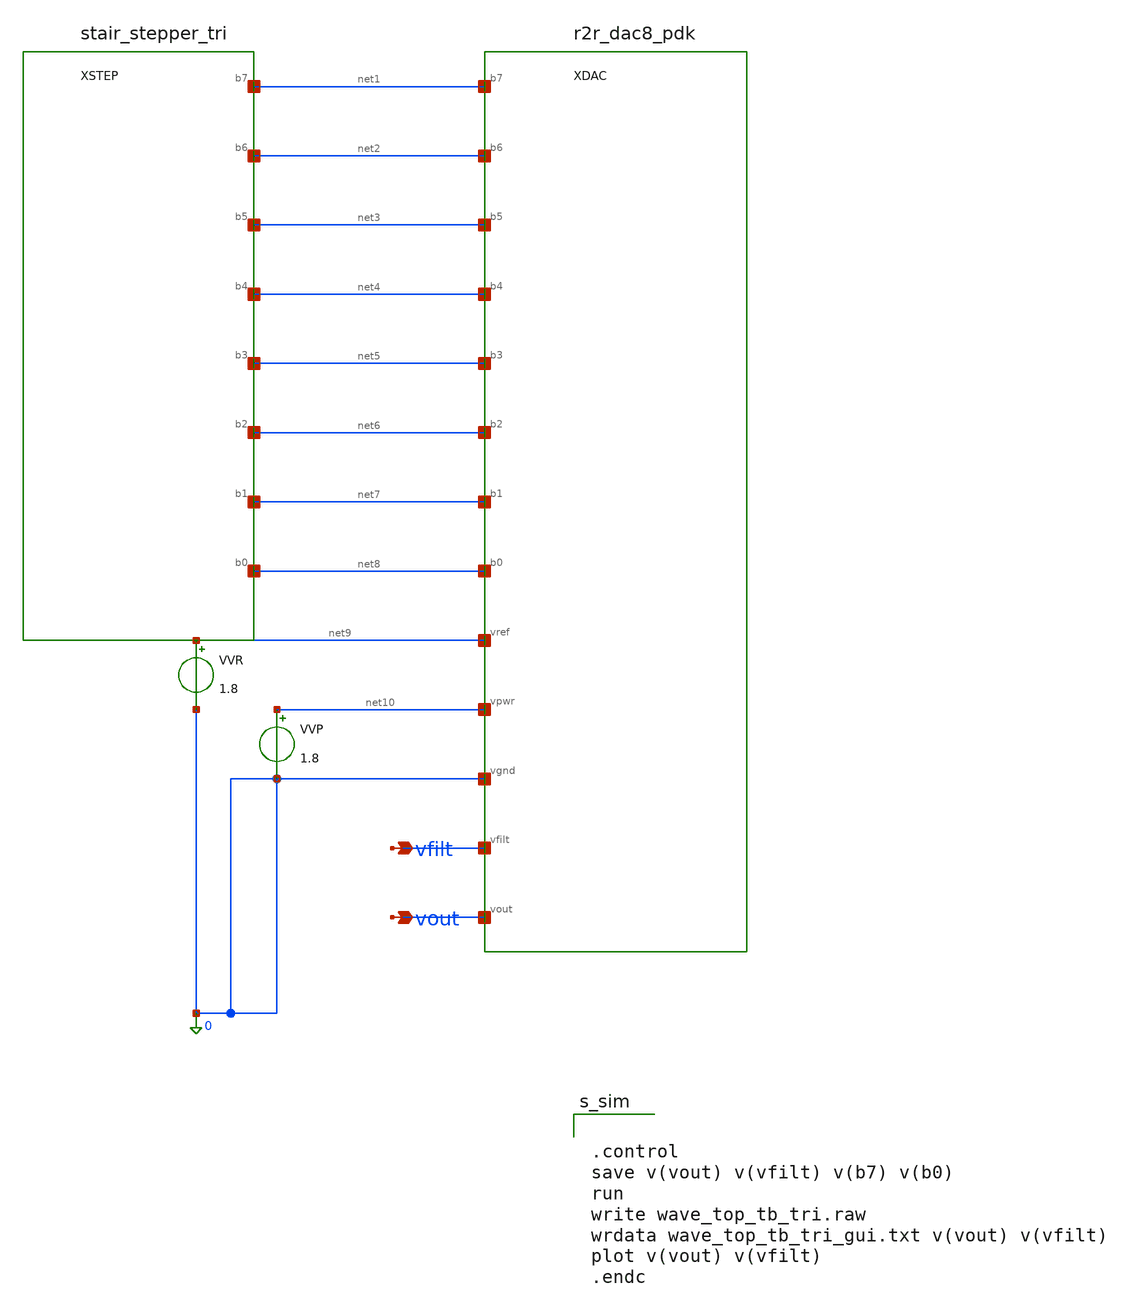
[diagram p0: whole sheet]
** sch_path: design/analog/xschem/wave_top_tb_tri.sch
**.subckt wave_top_tb_tri vfilt vout
*.opin vfilt
*.opin vout
XDAC net1 net2 net3 net4 net5 net6 net7 net8 net9 net10 0 vfilt vout r2r_dac8_pdk
XSTEP net1 net2 net3 net4 net5 net6 net7 net8 stair_stepper_tri
VVR net9 0 1.8
VVP net10 0 1.8
**** begin user architecture code

.lib /home/alrida-ismail/.local/share/pdk/sky130A/libs.tech/ngspice/sky130.lib.spice tt


.tran 100p 5.12e-06)


* tb: 256clk staircase replay of the RTL golden (see gen_tb_sch.py). Ctrl+click the launcher to load
*+ wave_top_tb_tri.raw into the embedded graph; batch proof (make tbexpand) reproduces results/tb_replay_tri.txt
*+ bit-identically



.control
save v(vout) v(vfilt) v(b7) v(b0)
run
write wave_top_tb_tri.raw
wrdata wave_top_tb_tri_gui.txt v(vout) v(vfilt)
plot v(vout) v(vfilt)
.endc


**** end user architecture code
**.ends

* expanding   symbol:  r2r_dac8_pdk.sym # of pins=13
** sym_path: design/analog/xschem/r2r_dac8_pdk.sym
** sch_path: design/analog/xschem/r2r_dac8_pdk.sch
.subckt r2r_dac8_pdk b7 b6 b5 b4 b3 b2 b1 b0 vref vpwr vgnd vfilt vout
*.ipin b7
*.ipin b6
*.ipin b5
*.ipin b4
*.ipin b3
*.ipin b2
*.ipin b1
*.ipin b0
*.ipin vref
*.ipin vpwr
*.ipin vgnd
*.opin vfilt
*.opin vout
XR76 n6 vout vgnd sky130_fd_pr__res_high_po W=4 L=357.43 mult=1 m=1
XR65 n5 n6 vgnd sky130_fd_pr__res_high_po W=4 L=357.43 mult=1 m=1
XR54 n4 n5 vgnd sky130_fd_pr__res_high_po W=4 L=357.43 mult=1 m=1
XR43 n3 n4 vgnd sky130_fd_pr__res_high_po W=4 L=357.43 mult=1 m=1
XR32 n2 n3 vgnd sky130_fd_pr__res_high_po W=4 L=357.43 mult=1 m=1
XR21 n1 n2 vgnd sky130_fd_pr__res_high_po W=4 L=357.43 mult=1 m=1
XR10 n0 n1 vgnd sky130_fd_pr__res_high_po W=4 L=357.43 mult=1 m=1
XRTERM vgnd n0 vgnd sky130_fd_pr__res_high_po W=4 L=716.98 mult=1 m=1
XR2B7 vout sw7 vgnd sky130_fd_pr__res_high_po W=4 L=716.98 mult=1 m=1
XMT1N7 sw7 b7 vref vgnd sky130_fd_pr__nfet_01v8 L=0.15 W=20 nf=1 ad='int((1 + 1)/2) * 20 / 1 * 0.29'
+ as='int((1 + 2)/2) * 20 / 1 * 0.29' pd='2*int((1 + 1)/2) * (20 / 1 + 0.29)' ps='2*int((1 + 2)/2) * (20 / 1 + 0.29)'
+ nrd='0.29 / 20 ' nrs='0.29 / 20 ' sa=0 sb=0 sd=0 mult=1 m=1
XMT1P7 vref b_n7 sw7 vref sky130_fd_pr__pfet_01v8 L=0.15 W=20 nf=1 ad='int((nf+1)/2) * W/nf * 0.29' as='int((nf+2)/2) * W/nf * 0.29'
+ pd='2*int((nf+1)/2) * (W/nf + 0.29)' ps='2*int((nf+2)/2) * (W/nf + 0.29)' nrd='0.29 / W' nrs='0.29 / W'
+ sa=0 sb=0 sd=0 mult=1 m=1
XMT2N7 sw7 b_n7 vgnd vgnd sky130_fd_pr__nfet_01v8 L=0.15 W=20 nf=1 ad='int((1 + 1)/2) * 20 / 1 * 0.29'
+ as='int((1 + 2)/2) * 20 / 1 * 0.29' pd='2*int((1 + 1)/2) * (20 / 1 + 0.29)' ps='2*int((1 + 2)/2) * (20 / 1 + 0.29)'
+ nrd='0.29 / 20 ' nrs='0.29 / 20 ' sa=0 sb=0 sd=0 mult=1 m=1
XMT2P7 vgnd b7 sw7 vref sky130_fd_pr__pfet_01v8 L=0.15 W=20 nf=1 ad='int((nf+1)/2) * W/nf * 0.29' as='int((nf+2)/2) * W/nf * 0.29'
+ pd='2*int((nf+1)/2) * (W/nf + 0.29)' ps='2*int((nf+2)/2) * (W/nf + 0.29)' nrd='0.29 / W' nrs='0.29 / W'
+ sa=0 sb=0 sd=0 mult=1 m=1
XMINVP7 b_n7 b7 vpwr vpwr sky130_fd_pr__pfet_01v8 L=0.15 W=1 nf=1 ad='int((nf+1)/2) * W/nf * 0.29' as='int((nf+2)/2) * W/nf * 0.29'
+ pd='2*int((nf+1)/2) * (W/nf + 0.29)' ps='2*int((nf+2)/2) * (W/nf + 0.29)' nrd='0.29 / W' nrs='0.29 / W'
+ sa=0 sb=0 sd=0 mult=1 m=1
XMINVN7 b_n7 b7 vgnd vgnd sky130_fd_pr__nfet_01v8 L=0.15 W=1 nf=1 ad='int((1 + 1)/2) * 1 / 1 * 0.29'
+ as='int((1 + 2)/2) * 1 / 1 * 0.29' pd='2*int((1 + 1)/2) * (1 / 1 + 0.29)' ps='2*int((1 + 2)/2) * (1 / 1 + 0.29)'
+ nrd='0.29 / 1 ' nrs='0.29 / 1 ' sa=0 sb=0 sd=0 mult=1 m=1
XR2B6 n6 sw6 vgnd sky130_fd_pr__res_high_po W=4 L=716.98 mult=1 m=1
XMT1N6 sw6 b6 vref vgnd sky130_fd_pr__nfet_01v8 L=0.15 W=20 nf=1 ad='int((1 + 1)/2) * 20 / 1 * 0.29'
+ as='int((1 + 2)/2) * 20 / 1 * 0.29' pd='2*int((1 + 1)/2) * (20 / 1 + 0.29)' ps='2*int((1 + 2)/2) * (20 / 1 + 0.29)'
+ nrd='0.29 / 20 ' nrs='0.29 / 20 ' sa=0 sb=0 sd=0 mult=1 m=1
XMT1P6 vref b_n6 sw6 vref sky130_fd_pr__pfet_01v8 L=0.15 W=20 nf=1 ad='int((nf+1)/2) * W/nf * 0.29' as='int((nf+2)/2) * W/nf * 0.29'
+ pd='2*int((nf+1)/2) * (W/nf + 0.29)' ps='2*int((nf+2)/2) * (W/nf + 0.29)' nrd='0.29 / W' nrs='0.29 / W'
+ sa=0 sb=0 sd=0 mult=1 m=1
XMT2N6 sw6 b_n6 vgnd vgnd sky130_fd_pr__nfet_01v8 L=0.15 W=20 nf=1 ad='int((1 + 1)/2) * 20 / 1 * 0.29'
+ as='int((1 + 2)/2) * 20 / 1 * 0.29' pd='2*int((1 + 1)/2) * (20 / 1 + 0.29)' ps='2*int((1 + 2)/2) * (20 / 1 + 0.29)'
+ nrd='0.29 / 20 ' nrs='0.29 / 20 ' sa=0 sb=0 sd=0 mult=1 m=1
XMT2P6 vgnd b6 sw6 vref sky130_fd_pr__pfet_01v8 L=0.15 W=20 nf=1 ad='int((nf+1)/2) * W/nf * 0.29' as='int((nf+2)/2) * W/nf * 0.29'
+ pd='2*int((nf+1)/2) * (W/nf + 0.29)' ps='2*int((nf+2)/2) * (W/nf + 0.29)' nrd='0.29 / W' nrs='0.29 / W'
+ sa=0 sb=0 sd=0 mult=1 m=1
XMINVP6 b_n6 b6 vpwr vpwr sky130_fd_pr__pfet_01v8 L=0.15 W=1 nf=1 ad='int((nf+1)/2) * W/nf * 0.29' as='int((nf+2)/2) * W/nf * 0.29'
+ pd='2*int((nf+1)/2) * (W/nf + 0.29)' ps='2*int((nf+2)/2) * (W/nf + 0.29)' nrd='0.29 / W' nrs='0.29 / W'
+ sa=0 sb=0 sd=0 mult=1 m=1
XMINVN6 b_n6 b6 vgnd vgnd sky130_fd_pr__nfet_01v8 L=0.15 W=1 nf=1 ad='int((1 + 1)/2) * 1 / 1 * 0.29'
+ as='int((1 + 2)/2) * 1 / 1 * 0.29' pd='2*int((1 + 1)/2) * (1 / 1 + 0.29)' ps='2*int((1 + 2)/2) * (1 / 1 + 0.29)'
+ nrd='0.29 / 1 ' nrs='0.29 / 1 ' sa=0 sb=0 sd=0 mult=1 m=1
XR2B5 n5 sw5 vgnd sky130_fd_pr__res_high_po W=4 L=716.98 mult=1 m=1
XMT1N5 sw5 b5 vref vgnd sky130_fd_pr__nfet_01v8 L=0.15 W=20 nf=1 ad='int((1 + 1)/2) * 20 / 1 * 0.29'
+ as='int((1 + 2)/2) * 20 / 1 * 0.29' pd='2*int((1 + 1)/2) * (20 / 1 + 0.29)' ps='2*int((1 + 2)/2) * (20 / 1 + 0.29)'
+ nrd='0.29 / 20 ' nrs='0.29 / 20 ' sa=0 sb=0 sd=0 mult=1 m=1
XMT1P5 vref b_n5 sw5 vref sky130_fd_pr__pfet_01v8 L=0.15 W=20 nf=1 ad='int((nf+1)/2) * W/nf * 0.29' as='int((nf+2)/2) * W/nf * 0.29'
+ pd='2*int((nf+1)/2) * (W/nf + 0.29)' ps='2*int((nf+2)/2) * (W/nf + 0.29)' nrd='0.29 / W' nrs='0.29 / W'
+ sa=0 sb=0 sd=0 mult=1 m=1
XMT2N5 sw5 b_n5 vgnd vgnd sky130_fd_pr__nfet_01v8 L=0.15 W=20 nf=1 ad='int((1 + 1)/2) * 20 / 1 * 0.29'
+ as='int((1 + 2)/2) * 20 / 1 * 0.29' pd='2*int((1 + 1)/2) * (20 / 1 + 0.29)' ps='2*int((1 + 2)/2) * (20 / 1 + 0.29)'
+ nrd='0.29 / 20 ' nrs='0.29 / 20 ' sa=0 sb=0 sd=0 mult=1 m=1
XMT2P5 vgnd b5 sw5 vref sky130_fd_pr__pfet_01v8 L=0.15 W=20 nf=1 ad='int((nf+1)/2) * W/nf * 0.29' as='int((nf+2)/2) * W/nf * 0.29'
+ pd='2*int((nf+1)/2) * (W/nf + 0.29)' ps='2*int((nf+2)/2) * (W/nf + 0.29)' nrd='0.29 / W' nrs='0.29 / W'
+ sa=0 sb=0 sd=0 mult=1 m=1
XMINVP5 b_n5 b5 vpwr vpwr sky130_fd_pr__pfet_01v8 L=0.15 W=1 nf=1 ad='int((nf+1)/2) * W/nf * 0.29' as='int((nf+2)/2) * W/nf * 0.29'
+ pd='2*int((nf+1)/2) * (W/nf + 0.29)' ps='2*int((nf+2)/2) * (W/nf + 0.29)' nrd='0.29 / W' nrs='0.29 / W'
+ sa=0 sb=0 sd=0 mult=1 m=1
XMINVN5 b_n5 b5 vgnd vgnd sky130_fd_pr__nfet_01v8 L=0.15 W=1 nf=1 ad='int((1 + 1)/2) * 1 / 1 * 0.29'
+ as='int((1 + 2)/2) * 1 / 1 * 0.29' pd='2*int((1 + 1)/2) * (1 / 1 + 0.29)' ps='2*int((1 + 2)/2) * (1 / 1 + 0.29)'
+ nrd='0.29 / 1 ' nrs='0.29 / 1 ' sa=0 sb=0 sd=0 mult=1 m=1
XR2B4 n4 sw4 vgnd sky130_fd_pr__res_high_po W=4 L=716.98 mult=1 m=1
XMT1N4 sw4 b4 vref vgnd sky130_fd_pr__nfet_01v8 L=0.15 W=20 nf=1 ad='int((1 + 1)/2) * 20 / 1 * 0.29'
+ as='int((1 + 2)/2) * 20 / 1 * 0.29' pd='2*int((1 + 1)/2) * (20 / 1 + 0.29)' ps='2*int((1 + 2)/2) * (20 / 1 + 0.29)'
+ nrd='0.29 / 20 ' nrs='0.29 / 20 ' sa=0 sb=0 sd=0 mult=1 m=1
XMT1P4 vref b_n4 sw4 vref sky130_fd_pr__pfet_01v8 L=0.15 W=20 nf=1 ad='int((nf+1)/2) * W/nf * 0.29' as='int((nf+2)/2) * W/nf * 0.29'
+ pd='2*int((nf+1)/2) * (W/nf + 0.29)' ps='2*int((nf+2)/2) * (W/nf + 0.29)' nrd='0.29 / W' nrs='0.29 / W'
+ sa=0 sb=0 sd=0 mult=1 m=1
XMT2N4 sw4 b_n4 vgnd vgnd sky130_fd_pr__nfet_01v8 L=0.15 W=20 nf=1 ad='int((1 + 1)/2) * 20 / 1 * 0.29'
+ as='int((1 + 2)/2) * 20 / 1 * 0.29' pd='2*int((1 + 1)/2) * (20 / 1 + 0.29)' ps='2*int((1 + 2)/2) * (20 / 1 + 0.29)'
+ nrd='0.29 / 20 ' nrs='0.29 / 20 ' sa=0 sb=0 sd=0 mult=1 m=1
XMT2P4 vgnd b4 sw4 vref sky130_fd_pr__pfet_01v8 L=0.15 W=20 nf=1 ad='int((nf+1)/2) * W/nf * 0.29' as='int((nf+2)/2) * W/nf * 0.29'
+ pd='2*int((nf+1)/2) * (W/nf + 0.29)' ps='2*int((nf+2)/2) * (W/nf + 0.29)' nrd='0.29 / W' nrs='0.29 / W'
+ sa=0 sb=0 sd=0 mult=1 m=1
XMINVP4 b_n4 b4 vpwr vpwr sky130_fd_pr__pfet_01v8 L=0.15 W=1 nf=1 ad='int((nf+1)/2) * W/nf * 0.29' as='int((nf+2)/2) * W/nf * 0.29'
+ pd='2*int((nf+1)/2) * (W/nf + 0.29)' ps='2*int((nf+2)/2) * (W/nf + 0.29)' nrd='0.29 / W' nrs='0.29 / W'
+ sa=0 sb=0 sd=0 mult=1 m=1
XMINVN4 b_n4 b4 vgnd vgnd sky130_fd_pr__nfet_01v8 L=0.15 W=1 nf=1 ad='int((1 + 1)/2) * 1 / 1 * 0.29'
+ as='int((1 + 2)/2) * 1 / 1 * 0.29' pd='2*int((1 + 1)/2) * (1 / 1 + 0.29)' ps='2*int((1 + 2)/2) * (1 / 1 + 0.29)'
+ nrd='0.29 / 1 ' nrs='0.29 / 1 ' sa=0 sb=0 sd=0 mult=1 m=1
XR2B3 n3 sw3 vgnd sky130_fd_pr__res_high_po W=4 L=716.98 mult=1 m=1
XMT1N3 sw3 b3 vref vgnd sky130_fd_pr__nfet_01v8 L=0.15 W=20 nf=1 ad='int((1 + 1)/2) * 20 / 1 * 0.29'
+ as='int((1 + 2)/2) * 20 / 1 * 0.29' pd='2*int((1 + 1)/2) * (20 / 1 + 0.29)' ps='2*int((1 + 2)/2) * (20 / 1 + 0.29)'
+ nrd='0.29 / 20 ' nrs='0.29 / 20 ' sa=0 sb=0 sd=0 mult=1 m=1
XMT1P3 vref b_n3 sw3 vref sky130_fd_pr__pfet_01v8 L=0.15 W=20 nf=1 ad='int((nf+1)/2) * W/nf * 0.29' as='int((nf+2)/2) * W/nf * 0.29'
+ pd='2*int((nf+1)/2) * (W/nf + 0.29)' ps='2*int((nf+2)/2) * (W/nf + 0.29)' nrd='0.29 / W' nrs='0.29 / W'
+ sa=0 sb=0 sd=0 mult=1 m=1
XMT2N3 sw3 b_n3 vgnd vgnd sky130_fd_pr__nfet_01v8 L=0.15 W=20 nf=1 ad='int((1 + 1)/2) * 20 / 1 * 0.29'
+ as='int((1 + 2)/2) * 20 / 1 * 0.29' pd='2*int((1 + 1)/2) * (20 / 1 + 0.29)' ps='2*int((1 + 2)/2) * (20 / 1 + 0.29)'
+ nrd='0.29 / 20 ' nrs='0.29 / 20 ' sa=0 sb=0 sd=0 mult=1 m=1
XMT2P3 vgnd b3 sw3 vref sky130_fd_pr__pfet_01v8 L=0.15 W=20 nf=1 ad='int((nf+1)/2) * W/nf * 0.29' as='int((nf+2)/2) * W/nf * 0.29'
+ pd='2*int((nf+1)/2) * (W/nf + 0.29)' ps='2*int((nf+2)/2) * (W/nf + 0.29)' nrd='0.29 / W' nrs='0.29 / W'
+ sa=0 sb=0 sd=0 mult=1 m=1
XMINVP3 b_n3 b3 vpwr vpwr sky130_fd_pr__pfet_01v8 L=0.15 W=1 nf=1 ad='int((nf+1)/2) * W/nf * 0.29' as='int((nf+2)/2) * W/nf * 0.29'
+ pd='2*int((nf+1)/2) * (W/nf + 0.29)' ps='2*int((nf+2)/2) * (W/nf + 0.29)' nrd='0.29 / W' nrs='0.29 / W'
+ sa=0 sb=0 sd=0 mult=1 m=1
XMINVN3 b_n3 b3 vgnd vgnd sky130_fd_pr__nfet_01v8 L=0.15 W=1 nf=1 ad='int((1 + 1)/2) * 1 / 1 * 0.29'
+ as='int((1 + 2)/2) * 1 / 1 * 0.29' pd='2*int((1 + 1)/2) * (1 / 1 + 0.29)' ps='2*int((1 + 2)/2) * (1 / 1 + 0.29)'
+ nrd='0.29 / 1 ' nrs='0.29 / 1 ' sa=0 sb=0 sd=0 mult=1 m=1
XR2B2 n2 sw2 vgnd sky130_fd_pr__res_high_po W=4 L=716.98 mult=1 m=1
XMT1N2 sw2 b2 vref vgnd sky130_fd_pr__nfet_01v8 L=0.15 W=20 nf=1 ad='int((1 + 1)/2) * 20 / 1 * 0.29'
+ as='int((1 + 2)/2) * 20 / 1 * 0.29' pd='2*int((1 + 1)/2) * (20 / 1 + 0.29)' ps='2*int((1 + 2)/2) * (20 / 1 + 0.29)'
+ nrd='0.29 / 20 ' nrs='0.29 / 20 ' sa=0 sb=0 sd=0 mult=1 m=1
XMT1P2 vref b_n2 sw2 vref sky130_fd_pr__pfet_01v8 L=0.15 W=20 nf=1 ad='int((nf+1)/2) * W/nf * 0.29' as='int((nf+2)/2) * W/nf * 0.29'
+ pd='2*int((nf+1)/2) * (W/nf + 0.29)' ps='2*int((nf+2)/2) * (W/nf + 0.29)' nrd='0.29 / W' nrs='0.29 / W'
+ sa=0 sb=0 sd=0 mult=1 m=1
XMT2N2 sw2 b_n2 vgnd vgnd sky130_fd_pr__nfet_01v8 L=0.15 W=20 nf=1 ad='int((1 + 1)/2) * 20 / 1 * 0.29'
+ as='int((1 + 2)/2) * 20 / 1 * 0.29' pd='2*int((1 + 1)/2) * (20 / 1 + 0.29)' ps='2*int((1 + 2)/2) * (20 / 1 + 0.29)'
+ nrd='0.29 / 20 ' nrs='0.29 / 20 ' sa=0 sb=0 sd=0 mult=1 m=1
XMT2P2 vgnd b2 sw2 vref sky130_fd_pr__pfet_01v8 L=0.15 W=20 nf=1 ad='int((nf+1)/2) * W/nf * 0.29' as='int((nf+2)/2) * W/nf * 0.29'
+ pd='2*int((nf+1)/2) * (W/nf + 0.29)' ps='2*int((nf+2)/2) * (W/nf + 0.29)' nrd='0.29 / W' nrs='0.29 / W'
+ sa=0 sb=0 sd=0 mult=1 m=1
XMINVP2 b_n2 b2 vpwr vpwr sky130_fd_pr__pfet_01v8 L=0.15 W=1 nf=1 ad='int((nf+1)/2) * W/nf * 0.29' as='int((nf+2)/2) * W/nf * 0.29'
+ pd='2*int((nf+1)/2) * (W/nf + 0.29)' ps='2*int((nf+2)/2) * (W/nf + 0.29)' nrd='0.29 / W' nrs='0.29 / W'
+ sa=0 sb=0 sd=0 mult=1 m=1
XMINVN2 b_n2 b2 vgnd vgnd sky130_fd_pr__nfet_01v8 L=0.15 W=1 nf=1 ad='int((1 + 1)/2) * 1 / 1 * 0.29'
+ as='int((1 + 2)/2) * 1 / 1 * 0.29' pd='2*int((1 + 1)/2) * (1 / 1 + 0.29)' ps='2*int((1 + 2)/2) * (1 / 1 + 0.29)'
+ nrd='0.29 / 1 ' nrs='0.29 / 1 ' sa=0 sb=0 sd=0 mult=1 m=1
XR2B1 n1 sw1 vgnd sky130_fd_pr__res_high_po W=4 L=716.98 mult=1 m=1
XMT1N1 sw1 b1 vref vgnd sky130_fd_pr__nfet_01v8 L=0.15 W=20 nf=1 ad='int((1 + 1)/2) * 20 / 1 * 0.29'
+ as='int((1 + 2)/2) * 20 / 1 * 0.29' pd='2*int((1 + 1)/2) * (20 / 1 + 0.29)' ps='2*int((1 + 2)/2) * (20 / 1 + 0.29)'
+ nrd='0.29 / 20 ' nrs='0.29 / 20 ' sa=0 sb=0 sd=0 mult=1 m=1
XMT1P1 vref b_n1 sw1 vref sky130_fd_pr__pfet_01v8 L=0.15 W=20 nf=1 ad='int((nf+1)/2) * W/nf * 0.29' as='int((nf+2)/2) * W/nf * 0.29'
+ pd='2*int((nf+1)/2) * (W/nf + 0.29)' ps='2*int((nf+2)/2) * (W/nf + 0.29)' nrd='0.29 / W' nrs='0.29 / W'
+ sa=0 sb=0 sd=0 mult=1 m=1
XMT2N1 sw1 b_n1 vgnd vgnd sky130_fd_pr__nfet_01v8 L=0.15 W=20 nf=1 ad='int((1 + 1)/2) * 20 / 1 * 0.29'
+ as='int((1 + 2)/2) * 20 / 1 * 0.29' pd='2*int((1 + 1)/2) * (20 / 1 + 0.29)' ps='2*int((1 + 2)/2) * (20 / 1 + 0.29)'
+ nrd='0.29 / 20 ' nrs='0.29 / 20 ' sa=0 sb=0 sd=0 mult=1 m=1
XMT2P1 vgnd b1 sw1 vref sky130_fd_pr__pfet_01v8 L=0.15 W=20 nf=1 ad='int((nf+1)/2) * W/nf * 0.29' as='int((nf+2)/2) * W/nf * 0.29'
+ pd='2*int((nf+1)/2) * (W/nf + 0.29)' ps='2*int((nf+2)/2) * (W/nf + 0.29)' nrd='0.29 / W' nrs='0.29 / W'
+ sa=0 sb=0 sd=0 mult=1 m=1
XMINVP1 b_n1 b1 vpwr vpwr sky130_fd_pr__pfet_01v8 L=0.15 W=1 nf=1 ad='int((nf+1)/2) * W/nf * 0.29' as='int((nf+2)/2) * W/nf * 0.29'
+ pd='2*int((nf+1)/2) * (W/nf + 0.29)' ps='2*int((nf+2)/2) * (W/nf + 0.29)' nrd='0.29 / W' nrs='0.29 / W'
+ sa=0 sb=0 sd=0 mult=1 m=1
XMINVN1 b_n1 b1 vgnd vgnd sky130_fd_pr__nfet_01v8 L=0.15 W=1 nf=1 ad='int((1 + 1)/2) * 1 / 1 * 0.29'
+ as='int((1 + 2)/2) * 1 / 1 * 0.29' pd='2*int((1 + 1)/2) * (1 / 1 + 0.29)' ps='2*int((1 + 2)/2) * (1 / 1 + 0.29)'
+ nrd='0.29 / 1 ' nrs='0.29 / 1 ' sa=0 sb=0 sd=0 mult=1 m=1
XR2B0 n0 sw0 vgnd sky130_fd_pr__res_high_po W=4 L=716.98 mult=1 m=1
XMT1N0 sw0 b0 vref vgnd sky130_fd_pr__nfet_01v8 L=0.15 W=20 nf=1 ad='int((1 + 1)/2) * 20 / 1 * 0.29'
+ as='int((1 + 2)/2) * 20 / 1 * 0.29' pd='2*int((1 + 1)/2) * (20 / 1 + 0.29)' ps='2*int((1 + 2)/2) * (20 / 1 + 0.29)'
+ nrd='0.29 / 20 ' nrs='0.29 / 20 ' sa=0 sb=0 sd=0 mult=1 m=1
XMT1P0 vref b_n0 sw0 vref sky130_fd_pr__pfet_01v8 L=0.15 W=20 nf=1 ad='int((nf+1)/2) * W/nf * 0.29' as='int((nf+2)/2) * W/nf * 0.29'
+ pd='2*int((nf+1)/2) * (W/nf + 0.29)' ps='2*int((nf+2)/2) * (W/nf + 0.29)' nrd='0.29 / W' nrs='0.29 / W'
+ sa=0 sb=0 sd=0 mult=1 m=1
XMT2N0 sw0 b_n0 vgnd vgnd sky130_fd_pr__nfet_01v8 L=0.15 W=20 nf=1 ad='int((1 + 1)/2) * 20 / 1 * 0.29'
+ as='int((1 + 2)/2) * 20 / 1 * 0.29' pd='2*int((1 + 1)/2) * (20 / 1 + 0.29)' ps='2*int((1 + 2)/2) * (20 / 1 + 0.29)'
+ nrd='0.29 / 20 ' nrs='0.29 / 20 ' sa=0 sb=0 sd=0 mult=1 m=1
XMT2P0 vgnd b0 sw0 vref sky130_fd_pr__pfet_01v8 L=0.15 W=20 nf=1 ad='int((nf+1)/2) * W/nf * 0.29' as='int((nf+2)/2) * W/nf * 0.29'
+ pd='2*int((nf+1)/2) * (W/nf + 0.29)' ps='2*int((nf+2)/2) * (W/nf + 0.29)' nrd='0.29 / W' nrs='0.29 / W'
+ sa=0 sb=0 sd=0 mult=1 m=1
XMINVP0 b_n0 b0 vpwr vpwr sky130_fd_pr__pfet_01v8 L=0.15 W=1 nf=1 ad='int((nf+1)/2) * W/nf * 0.29' as='int((nf+2)/2) * W/nf * 0.29'
+ pd='2*int((nf+1)/2) * (W/nf + 0.29)' ps='2*int((nf+2)/2) * (W/nf + 0.29)' nrd='0.29 / W' nrs='0.29 / W'
+ sa=0 sb=0 sd=0 mult=1 m=1
XMINVN0 b_n0 b0 vgnd vgnd sky130_fd_pr__nfet_01v8 L=0.15 W=1 nf=1 ad='int((1 + 1)/2) * 1 / 1 * 0.29'
+ as='int((1 + 2)/2) * 1 / 1 * 0.29' pd='2*int((1 + 1)/2) * (1 / 1 + 0.29)' ps='2*int((1 + 2)/2) * (1 / 1 + 0.29)'
+ nrd='0.29 / 1 ' nrs='0.29 / 1 ' sa=0 sb=0 sd=0 mult=1 m=1
XRFILT vout vfilt vgnd sky130_fd_pr__res_high_po W=1 L=89.36 mult=1 m=1
XCFLT vfilt vgnd sky130_fd_pr__cap_mim_m3_1 W=15 L=15 MF=1 m=1
.ends


* expanding   symbol:  stair_stepper_tri.sym # of pins=8
** sym_path: design/analog/xschem/stair_stepper_tri.sym
** sch_path: design/analog/xschem/stair_stepper_tri.sch
.subckt stair_stepper_tri b7 b6 b5 b4 b3 b2 b1 b0
*.opin b7
*.opin b6
*.opin b5
*.opin b4
*.opin b3
*.opin b2
*.opin b1
*.opin b0
Vb7 b7 0 pwl(0 0.0 1.2795e-06 0.0 1.28e-06 1.8 3.8395e-06 1.8 3.84e-06 0.0 5.12e-06 0.0)
Vb6 b6 0 pwl(0 0.0 6.395e-07 0.0 6.4e-07 1.8 1.2795e-06 1.8 1.28e-06 0.0 1.9195e-06 0.0 1.92e-06 1.8
+ 3.1995e-06 1.8 3.2e-06 0.0 3.8395e-06 0.0 3.84e-06 1.8 4.4795e-06 1.8 4.48e-06 0.0 5.12e-06 0.0)
Vb5 b5 0 pwl(0 0.0 3.195e-07 0.0 3.2e-07 1.8 6.395e-07 1.8 6.4e-07 0.0 9.595e-07 0.0 9.6e-07 1.8
+ 1.2795e-06 1.8 1.28e-06 0.0 1.5995e-06 0.0 1.6e-06 1.8 1.9195e-06 1.8 1.92e-06 0.0 2.2395e-06 0.0 2.24e-06 1.8
+ 2.8795e-06 1.8 2.88e-06 0.0 3.1995e-06 0.0 3.2e-06 1.8 3.5195e-06 1.8 3.52e-06 0.0 3.8395e-06 0.0 3.84e-06 1.8
+ 4.1595e-06 1.8 4.16e-06 0.0 4.4795e-06 0.0 4.48e-06 1.8 4.7995e-06 1.8 4.8e-06 0.0 5.12e-06 0.0)
Vb4 b4 0 pwl(0 0.0 1.595e-07 0.0 1.6e-07 1.8 3.195e-07 1.8 3.2e-07 0.0 4.795e-07 0.0 4.8e-07 1.8
+ 6.395e-07 1.8 6.4e-07 0.0 7.995e-07 0.0 8e-07 1.8 9.595e-07 1.8 9.6e-07 0.0 1.1195e-06 0.0 1.12e-06 1.8
+ 1.2795e-06 1.8 1.28e-06 0.0 1.4395e-06 0.0 1.44e-06 1.8 1.5995e-06 1.8 1.6e-06 0.0 1.7595e-06 0.0 1.76e-06 1.8
+ 1.9195e-06 1.8 1.92e-06 0.0 2.0795e-06 0.0 2.08e-06 1.8 2.2395e-06 1.8 2.24e-06 0.0 2.3995e-06 0.0 2.4e-06 1.8
+ 2.7195e-06 1.8 2.72e-06 0.0 2.8795e-06 0.0 2.88e-06 1.8 3.0395e-06 1.8 3.04e-06 0.0 3.1995e-06 0.0 3.2e-06 1.8
+ 3.3595e-06 1.8 3.36e-06 0.0 3.5195e-06 0.0 3.52e-06 1.8 3.6795e-06 1.8 3.68e-06 0.0 3.8395e-06 0.0 3.84e-06
+ 1.8 3.9995e-06 1.8 4e-06 0.0 4.1595e-06 0.0 4.16e-06 1.8 4.3195e-06 1.8 4.32e-06 0.0 4.4795e-06 0.0
+ 4.48e-06 1.8 4.6395e-06 1.8 4.64e-06 0.0 4.7995e-06 0.0 4.8e-06 1.8 4.9595e-06 1.8 4.96e-06 0.0 5.12e-06
+ 0.0)
Vb3 b3 0 pwl(0 0.0 7.95e-08 0.0 8e-08 1.8 1.595e-07 1.8 1.6e-07 0.0 2.395e-07 0.0 2.4e-07 1.8
+ 3.195e-07 1.8 3.2e-07 0.0 3.995e-07 0.0 4e-07 1.8 4.795e-07 1.8 4.8e-07 0.0 5.595e-07 0.0 5.6e-07 1.8
+ 6.395e-07 1.8 6.4e-07 0.0 7.195e-07 0.0 7.2e-07 1.8 7.995e-07 1.8 8e-07 0.0 8.795e-07 0.0 8.8e-07 1.8
+ 9.595e-07 1.8 9.6e-07 0.0 1.0395e-06 0.0 1.04e-06 1.8 1.1195e-06 1.8 1.12e-06 0.0 1.1995e-06 0.0 1.2e-06 1.8
+ 1.2795e-06 1.8 1.28e-06 0.0 1.3595e-06 0.0 1.36e-06 1.8 1.4395e-06 1.8 1.44e-06 0.0 1.5195e-06 0.0 1.52e-06
+ 1.8 1.5995e-06 1.8 1.6e-06 0.0 1.6795e-06 0.0 1.68e-06 1.8 1.7595e-06 1.8 1.76e-06 0.0 1.8395e-06 0.0
+ 1.84e-06 1.8 1.9195e-06 1.8 1.92e-06 0.0 1.9995e-06 0.0 2e-06 1.8 2.0795e-06 1.8 2.08e-06 0.0 2.1595e-06 0.0
+ 2.16e-06 1.8 2.2395e-06 1.8 2.24e-06 0.0 2.3195e-06 0.0 2.32e-06 1.8 2.3995e-06 1.8 2.4e-06 0.0 2.4795e-06
+ 0.0 2.48e-06 1.8 2.6395e-06 1.8 2.64e-06 0.0 2.7195e-06 0.0 2.72e-06 1.8 2.7995e-06 1.8 2.8e-06 0.0
+ 2.8795e-06 0.0 2.88e-06 1.8 2.9595e-06 1.8 2.96e-06 0.0 3.0395e-06 0.0 3.04e-06 1.8 3.1195e-06 1.8 3.12e-06
+ 0.0 3.1995e-06 0.0 3.2e-06 1.8 3.2795e-06 1.8 3.28e-06 0.0 3.3595e-06 0.0 3.36e-06 1.8 3.4395e-06 1.8
+ 3.44e-06 0.0 3.5195e-06 0.0 3.52e-06 1.8 3.5995e-06 1.8 3.6e-06 0.0 3.6795e-06 0.0 3.68e-06 1.8 3.7595e-06
+ 1.8 3.76e-06 0.0 3.8395e-06 0.0 3.84e-06 1.8 3.9195e-06 1.8 3.92e-06 0.0 3.9995e-06 0.0 4e-06 1.8
+ 4.0795e-06 1.8 4.08e-06 0.0 4.1595e-06 0.0 4.16e-06 1.8 4.2395e-06 1.8 4.24e-06 0.0 4.3195e-06 0.0 4.32e-06
+ 1.8 4.3995e-06 1.8 4.4e-06 0.0 4.4795e-06 0.0 4.48e-06 1.8 4.5595e-06 1.8 4.56e-06 0.0 4.6395e-06 0.0
+ 4.64e-06 1.8 4.7195e-06 1.8 4.72e-06 0.0 4.7995e-06 0.0 4.8e-06 1.8 4.8795e-06 1.8 4.88e-06 0.0 4.9595e-06
+ 0.0 4.96e-06 1.8 5.0395e-06 1.8 5.04e-06 0.0 5.12e-06 0.0)
Vb2 b2 0 pwl(0 0.0 3.95e-08 0.0 4e-08 1.8 7.95e-08 1.8 8e-08 0.0 1.195e-07 0.0 1.2e-07 1.8 1.595e-07
+ 1.8 1.6e-07 0.0 1.995e-07 0.0 2e-07 1.8 2.395e-07 1.8 2.4e-07 0.0 2.795e-07 0.0 2.8e-07 1.8 3.195e-07
+ 1.8 3.2e-07 0.0 3.595e-07 0.0 3.6e-07 1.8 3.995e-07 1.8 4e-07 0.0 4.395e-07 0.0 4.4e-07 1.8 4.795e-07
+ 1.8 4.8e-07 0.0 5.195e-07 0.0 5.2e-07 1.8 5.595e-07 1.8 5.6e-07 0.0 5.995e-07 0.0 6e-07 1.8 6.395e-07
+ 1.8 6.4e-07 0.0 6.795e-07 0.0 6.8e-07 1.8 7.195e-07 1.8 7.2e-07 0.0 7.595e-07 0.0 7.6e-07 1.8 7.995e-07
+ 1.8 8e-07 0.0 8.395e-07 0.0 8.4e-07 1.8 8.795e-07 1.8 8.8e-07 0.0 9.195e-07 0.0 9.2e-07 1.8 9.595e-07
+ 1.8 9.6e-07 0.0 9.995e-07 0.0 1e-06 1.8 1.0395e-06 1.8 1.04e-06 0.0 1.0795e-06 0.0 1.08e-06 1.8
+ 1.1195e-06 1.8 1.12e-06 0.0 1.1595e-06 0.0 1.16e-06 1.8 1.1995e-06 1.8 1.2e-06 0.0 1.2395e-06 0.0 1.24e-06 1.8
+ 1.2795e-06 1.8 1.28e-06 0.0 1.3195e-06 0.0 1.32e-06 1.8 1.3595e-06 1.8 1.36e-06 0.0 1.3995e-06 0.0 1.4e-06 1.8
+ 1.4395e-06 1.8 1.44e-06 0.0 1.4795e-06 0.0 1.48e-06 1.8 1.5195e-06 1.8 1.52e-06 0.0 1.5595e-06 0.0 1.56e-06
+ 1.8 1.5995e-06 1.8 1.6e-06 0.0 1.6395e-06 0.0 1.64e-06 1.8 1.6795e-06 1.8 1.68e-06 0.0 1.7195e-06 0.0
+ 1.72e-06 1.8 1.7595e-06 1.8 1.76e-06 0.0 1.7995e-06 0.0 1.8e-06 1.8 1.8395e-06 1.8 1.84e-06 0.0 1.8795e-06
+ 0.0 1.88e-06 1.8 1.9195e-06 1.8 1.92e-06 0.0 1.9595e-06 0.0 1.96e-06 1.8 1.9995e-06 1.8 2e-06 0.0
+ 2.0395e-06 0.0 2.04e-06 1.8 2.0795e-06 1.8 2.08e-06 0.0 2.1195e-06 0.0 2.12e-06 1.8 2.1595e-06 1.8 2.16e-06
+ 0.0 2.1995e-06 0.0 2.2e-06 1.8 2.2395e-06 1.8 2.24e-06 0.0 2.2795e-06 0.0 2.28e-06 1.8 2.3195e-06 1.8
+ 2.32e-06 0.0 2.3595e-06 0.0 2.36e-06 1.8 2.3995e-06 1.8 2.4e-06 0.0 2.4395e-06 0.0 2.44e-06 1.8 2.4795e-06
+ 1.8 2.48e-06 0.0 2.5195e-06 0.0 2.52e-06 1.8 2.5995e-06 1.8 2.6e-06 0.0 2.6395e-06 0.0 2.64e-06 1.8
+ 2.6795e-06 1.8 2.68e-06 0.0 2.7195e-06 0.0 2.72e-06 1.8 2.7595e-06 1.8 2.76e-06 0.0 2.7995e-06 0.0 2.8e-06 1.8
+ 2.8395e-06 1.8 2.84e-06 0.0 2.8795e-06 0.0 2.88e-06 1.8 2.9195e-06 1.8 2.92e-06 0.0 2.9595e-06 0.0 2.96e-06
+ 1.8 2.9995e-06 1.8 3e-06 0.0 3.0395e-06 0.0 3.04e-06 1.8 3.0795e-06 1.8 3.08e-06 0.0 3.1195e-06 0.0
+ 3.12e-06 1.8 3.1595e-06 1.8 3.16e-06 0.0 3.1995e-06 0.0 3.2e-06 1.8 3.2395e-06 1.8 3.24e-06 0.0 3.2795e-06
+ 0.0 3.28e-06 1.8 3.3195e-06 1.8 3.32e-06 0.0 3.3595e-06 0.0 3.36e-06 1.8 3.3995e-06 1.8 3.4e-06 0.0
+ 3.4395e-06 0.0 3.44e-06 1.8 3.4795e-06 1.8 3.48e-06 0.0 3.5195e-06 0.0 3.52e-06 1.8 3.5595e-06 1.8 3.56e-06
+ 0.0 3.5995e-06 0.0 3.6e-06 1.8 3.6395e-06 1.8 3.64e-06 0.0 3.6795e-06 0.0 3.68e-06 1.8 3.7195e-06 1.8
+ 3.72e-06 0.0 3.7595e-06 0.0 3.76e-06 1.8 3.7995e-06 1.8 3.8e-06 0.0 3.8395e-06 0.0 3.84e-06 1.8 3.8795e-06
+ 1.8 3.88e-06 0.0 3.9195e-06 0.0 3.92e-06 1.8 3.9595e-06 1.8 3.96e-06 0.0 3.9995e-06 0.0 4e-06 1.8
+ 4.0395e-06 1.8 4.04e-06 0.0 4.0795e-06 0.0 4.08e-06 1.8 4.1195e-06 1.8 4.12e-06 0.0 4.1595e-06 0.0 4.16e-06
+ 1.8 4.1995e-06 1.8 4.2e-06 0.0 4.2395e-06 0.0 4.24e-06 1.8 4.2795e-06 1.8 4.28e-06 0.0 4.3195e-06 0.0
+ 4.32e-06 1.8 4.3595e-06 1.8 4.36e-06 0.0 4.3995e-06 0.0 4.4e-06 1.8 4.4395e-06 1.8 4.44e-06 0.0 4.4795e-06
+ 0.0 4.48e-06 1.8 4.5195e-06 1.8 4.52e-06 0.0 4.5595e-06 0.0 4.56e-06 1.8 4.5995e-06 1.8 4.6e-06 0.0
+ 4.6395e-06 0.0 4.64e-06 1.8 4.6795e-06 1.8 4.68e-06 0.0 4.7195e-06 0.0 4.72e-06 1.8 4.7595e-06 1.8 4.76e-06
+ 0.0 4.7995e-06 0.0 4.8e-06 1.8 4.8395e-06 1.8 4.84e-06 0.0 4.8795e-06 0.0 4.88e-06 1.8 4.9195e-06 1.8
+ 4.92e-06 0.0 4.9595e-06 0.0 4.96e-06 1.8 4.9995e-06 1.8 5e-06 0.0 5.0395e-06 0.0 5.04e-06 1.8 5.0795e-06 1.8
+ 5.08e-06 0.0 5.12e-06 0.0)
Vb1 b1 0 pwl(0 0.0 1.95e-08 0.0 2e-08 1.8 3.95e-08 1.8 4e-08 0.0 5.95e-08 0.0 6e-08 1.8 7.95e-08 1.8
+ 8e-08 0.0 9.95e-08 0.0 1e-07 1.8 1.195e-07 1.8 1.2e-07 0.0 1.395e-07 0.0 1.4e-07 1.8 1.595e-07 1.8
+ 1.6e-07 0.0 1.795e-07 0.0 1.8e-07 1.8 1.995e-07 1.8 2e-07 0.0 2.195e-07 0.0 2.2e-07 1.8 2.395e-07 1.8
+ 2.4e-07 0.0 2.595e-07 0.0 2.6e-07 1.8 2.795e-07 1.8 2.8e-07 0.0 2.995e-07 0.0 3e-07 1.8 3.195e-07 1.8
+ 3.2e-07 0.0 3.395e-07 0.0 3.4e-07 1.8 3.595e-07 1.8 3.6e-07 0.0 3.795e-07 0.0 3.8e-07 1.8 3.995e-07 1.8
+ 4e-07 0.0 4.195e-07 0.0 4.2e-07 1.8 4.395e-07 1.8 4.4e-07 0.0 4.595e-07 0.0 4.6e-07 1.8 4.795e-07 1.8
+ 4.8e-07 0.0 4.995e-07 0.0 5e-07 1.8 5.195e-07 1.8 5.2e-07 0.0 5.395e-07 0.0 5.4e-07 1.8 5.595e-07 1.8
+ 5.6e-07 0.0 5.795e-07 0.0 5.8e-07 1.8 5.995e-07 1.8 6e-07 0.0 6.195e-07 0.0 6.2e-07 1.8 6.395e-07 1.8
+ 6.4e-07 0.0 6.595e-07 0.0 6.6e-07 1.8 6.795e-07 1.8 6.8e-07 0.0 6.995e-07 0.0 7e-07 1.8 7.195e-07 1.8
+ 7.2e-07 0.0 7.395e-07 0.0 7.4e-07 1.8 7.595e-07 1.8 7.6e-07 0.0 7.795e-07 0.0 7.8e-07 1.8 7.995e-07 1.8
+ 8e-07 0.0 8.195e-07 0.0 8.2e-07 1.8 8.395e-07 1.8 8.4e-07 0.0 8.595e-07 0.0 8.6e-07 1.8 8.795e-07 1.8
+ 8.8e-07 0.0 8.995e-07 0.0 9e-07 1.8 9.195e-07 1.8 9.2e-07 0.0 9.395e-07 0.0 9.4e-07 1.8 9.595e-07 1.8
+ 9.6e-07 0.0 9.795e-07 0.0 9.8e-07 1.8 9.995e-07 1.8 1e-06 0.0 1.0195e-06 0.0 1.02e-06 1.8 1.0395e-06 1.8
+ 1.04e-06 0.0 1.0595e-06 0.0 1.06e-06 1.8 1.0795e-06 1.8 1.08e-06 0.0 1.0995e-06 0.0 1.1e-06 1.8 1.1195e-06
+ 1.8 1.12e-06 0.0 1.1395e-06 0.0 1.14e-06 1.8 1.1595e-06 1.8 1.16e-06 0.0 1.1795e-06 0.0 1.18e-06 1.8
+ 1.1995e-06 1.8 1.2e-06 0.0 1.2195e-06 0.0 1.22e-06 1.8 1.2395e-06 1.8 1.24e-06 0.0 1.2595e-06 0.0 1.26e-06 1.8
+ 1.2795e-06 1.8 1.28e-06 0.0 1.2995e-06 0.0 1.3e-06 1.8 1.3195e-06 1.8 1.32e-06 0.0 1.3395e-06 0.0 1.34e-06 1.8
+ 1.3595e-06 1.8 1.36e-06 0.0 1.3795e-06 0.0 1.38e-06 1.8 1.3995e-06 1.8 1.4e-06 0.0 1.4195e-06 0.0 1.42e-06 1.8
+ 1.4395e-06 1.8 1.44e-06 0.0 1.4595e-06 0.0 1.46e-06 1.8 1.4795e-06 1.8 1.48e-06 0.0 1.4995e-06 0.0 1.5e-06 1.8
+ 1.5195e-06 1.8 1.52e-06 0.0 1.5395e-06 0.0 1.54e-06 1.8 1.5595e-06 1.8 1.56e-06 0.0 1.5795e-06 0.0 1.58e-06
+ 1.8 1.5995e-06 1.8 1.6e-06 0.0 1.6195e-06 0.0 1.62e-06 1.8 1.6395e-06 1.8 1.64e-06 0.0 1.6595e-06 0.0
+ 1.66e-06 1.8 1.6795e-06 1.8 1.68e-06 0.0 1.6995e-06 0.0 1.7e-06 1.8 1.7195e-06 1.8 1.72e-06 0.0 1.7395e-06
+ 0.0 1.74e-06 1.8 1.7595e-06 1.8 1.76e-06 0.0 1.7795e-06 0.0 1.78e-06 1.8 1.7995e-06 1.8 1.8e-06 0.0
+ 1.8195e-06 0.0 1.82e-06 1.8 1.8395e-06 1.8 1.84e-06 0.0 1.8595e-06 0.0 1.86e-06 1.8 1.8795e-06 1.8 1.88e-06
+ 0.0 1.8995e-06 0.0 1.9e-06 1.8 1.9195e-06 1.8 1.92e-06 0.0 1.9395e-06 0.0 1.94e-06 1.8 1.9595e-06 1.8
+ 1.96e-06 0.0 1.9795e-06 0.0 1.98e-06 1.8 1.9995e-06 1.8 2e-06 0.0 2.0195e-06 0.0 2.02e-06 1.8 2.0395e-06 1.8
+ 2.04e-06 0.0 2.0595e-06 0.0 2.06e-06 1.8 2.0795e-06 1.8 2.08e-06 0.0 2.0995e-06 0.0 2.1e-06 1.8 2.1195e-06
+ 1.8 2.12e-06 0.0 2.1395e-06 0.0 2.14e-06 1.8 2.1595e-06 1.8 2.16e-06 0.0 2.1795e-06 0.0 2.18e-06 1.8
+ 2.1995e-06 1.8 2.2e-06 0.0 2.2195e-06 0.0 2.22e-06 1.8 2.2395e-06 1.8 2.24e-06 0.0 2.2595e-06 0.0 2.26e-06 1.8
+ 2.2795e-06 1.8 2.28e-06 0.0 2.2995e-06 0.0 2.3e-06 1.8 2.3195e-06 1.8 2.32e-06 0.0 2.3395e-06 0.0 2.34e-06 1.8
+ 2.3595e-06 1.8 2.36e-06 0.0 2.3795e-06 0.0 2.38e-06 1.8 2.3995e-06 1.8 2.4e-06 0.0 2.4195e-06 0.0 2.42e-06 1.8
+ 2.4395e-06 1.8 2.44e-06 0.0 2.4595e-06 0.0 2.46e-06 1.8 2.4795e-06 1.8 2.48e-06 0.0 2.4995e-06 0.0 2.5e-06 1.8
+ 2.5195e-06 1.8 2.52e-06 0.0 2.5395e-06 0.0 2.54e-06 1.8 2.5795e-06 1.8 2.58e-06 0.0 2.5995e-06 0.0 2.6e-06 1.8
+ 2.6195e-06 1.8 2.62e-06 0.0 2.6395e-06 0.0 2.64e-06 1.8 2.6595e-06 1.8 2.66e-06 0.0 2.6795e-06 0.0 2.68e-06
+ 1.8 2.6995e-06 1.8 2.7e-06 0.0 2.7195e-06 0.0 2.72e-06 1.8 2.7395e-06 1.8 2.74e-06 0.0 2.7595e-06 0.0
+ 2.76e-06 1.8 2.7795e-06 1.8 2.78e-06 0.0 2.7995e-06 0.0 2.8e-06 1.8 2.8195e-06 1.8 2.82e-06 0.0 2.8395e-06
+ 0.0 2.84e-06 1.8 2.8595e-06 1.8 2.86e-06 0.0 2.8795e-06 0.0 2.88e-06 1.8 2.8995e-06 1.8 2.9e-06 0.0
+ 2.9195e-06 0.0 2.92e-06 1.8 2.9395e-06 1.8 2.94e-06 0.0 2.9595e-06 0.0 2.96e-06 1.8 2.9795e-06 1.8 2.98e-06
+ 0.0 2.9995e-06 0.0 3e-06 1.8 3.0195e-06 1.8 3.02e-06 0.0 3.0395e-06 0.0 3.04e-06 1.8 3.0595e-06 1.8
+ 3.06e-06 0.0 3.0795e-06 0.0 3.08e-06 1.8 3.0995e-06 1.8 3.1e-06 0.0 3.1195e-06 0.0 3.12e-06 1.8 3.1395e-06
+ 1.8 3.14e-06 0.0 3.1595e-06 0.0 3.16e-06 1.8 3.1795e-06 1.8 3.18e-06 0.0 3.1995e-06 0.0 3.2e-06 1.8
+ 3.2195e-06 1.8 3.22e-06 0.0 3.2395e-06 0.0 3.24e-06 1.8 3.2595e-06 1.8 3.26e-06 0.0 3.2795e-06 0.0 3.28e-06
+ 1.8 3.2995e-06 1.8 3.3e-06 0.0 3.3195e-06 0.0 3.32e-06 1.8 3.3395e-06 1.8 3.34e-06 0.0 3.3595e-06 0.0
+ 3.36e-06 1.8 3.3795e-06 1.8 3.38e-06 0.0 3.3995e-06 0.0 3.4e-06 1.8 3.4195e-06 1.8 3.42e-06 0.0 3.4395e-06
+ 0.0 3.44e-06 1.8 3.4595e-06 1.8 3.46e-06 0.0 3.4795e-06 0.0 3.48e-06 1.8 3.4995e-06 1.8 3.5e-06 0.0
+ 3.5195e-06 0.0 3.52e-06 1.8 3.5395e-06 1.8 3.54e-06 0.0 3.5595e-06 0.0 3.56e-06 1.8 3.5795e-06 1.8 3.58e-06
+ 0.0 3.5995e-06 0.0 3.6e-06 1.8 3.6195e-06 1.8 3.62e-06 0.0 3.6395e-06 0.0 3.64e-06 1.8 3.6595e-06 1.8
+ 3.66e-06 0.0 3.6795e-06 0.0 3.68e-06 1.8 3.6995e-06 1.8 3.7e-06 0.0 3.7195e-06 0.0 3.72e-06 1.8 3.7395e-06
+ 1.8 3.74e-06 0.0 3.7595e-06 0.0 3.76e-06 1.8 3.7795e-06 1.8 3.78e-06 0.0 3.7995e-06 0.0 3.8e-06 1.8
+ 3.8195e-06 1.8 3.82e-06 0.0 3.8395e-06 0.0 3.84e-06 1.8 3.8595e-06 1.8 3.86e-06 0.0 3.8795e-06 0.0 3.88e-06
+ 1.8 3.8995e-06 1.8 3.9e-06 0.0 3.9195e-06 0.0 3.92e-06 1.8 3.9395e-06 1.8 3.94e-06 0.0 3.9595e-06 0.0
+ 3.96e-06 1.8 3.9795e-06 1.8 3.98e-06 0.0 3.9995e-06 0.0 4e-06 1.8 4.0195e-06 1.8 4.02e-06 0.0 4.0395e-06 0.0
+ 4.04e-06 1.8 4.0595e-06 1.8 4.06e-06 0.0 4.0795e-06 0.0 4.08e-06 1.8 4.0995e-06 1.8 4.1e-06 0.0 4.1195e-06
+ 0.0 4.12e-06 1.8 4.1395e-06 1.8 4.14e-06 0.0 4.1595e-06 0.0 4.16e-06 1.8 4.1795e-06 1.8 4.18e-06 0.0
+ 4.1995e-06 0.0 4.2e-06 1.8 4.2195e-06 1.8 4.22e-06 0.0 4.2395e-06 0.0 4.24e-06 1.8 4.2595e-06 1.8 4.26e-06 0.0
+ 4.2795e-06 0.0 4.28e-06 1.8 4.2995e-06 1.8 4.3e-06 0.0 4.3195e-06 0.0 4.32e-06 1.8 4.3395e-06 1.8 4.34e-06 0.0
+ 4.3595e-06 0.0 4.36e-06 1.8 4.3795e-06 1.8 4.38e-06 0.0 4.3995e-06 0.0 4.4e-06 1.8 4.4195e-06 1.8 4.42e-06 0.0
+ 4.4395e-06 0.0 4.44e-06 1.8 4.4595e-06 1.8 4.46e-06 0.0 4.4795e-06 0.0 4.48e-06 1.8 4.4995e-06 1.8 4.5e-06 0.0
+ 4.5195e-06 0.0 4.52e-06 1.8 4.5395e-06 1.8 4.54e-06 0.0 4.5595e-06 0.0 4.56e-06 1.8 4.5795e-06 1.8 4.58e-06
+ 0.0 4.5995e-06 0.0 4.6e-06 1.8 4.6195e-06 1.8 4.62e-06 0.0 4.6395e-06 0.0 4.64e-06 1.8 4.6595e-06 1.8
+ 4.66e-06 0.0 4.6795e-06 0.0 4.68e-06 1.8 4.6995e-06 1.8 4.7e-06 0.0 4.7195e-06 0.0 4.72e-06 1.8 4.7395e-06
+ 1.8 4.74e-06 0.0 4.7595e-06 0.0 4.76e-06 1.8 4.7795e-06 1.8 4.78e-06 0.0 4.7995e-06 0.0 4.8e-06 1.8
+ 4.8195e-06 1.8 4.82e-06 0.0 4.8395e-06 0.0 4.84e-06 1.8 4.8595e-06 1.8 4.86e-06 0.0 4.8795e-06 0.0 4.88e-06
+ 1.8 4.8995e-06 1.8 4.9e-06 0.0 4.9195e-06 0.0 4.92e-06 1.8 4.9395e-06 1.8 4.94e-06 0.0 4.9595e-06 0.0
+ 4.96e-06 1.8 4.9795e-06 1.8 4.98e-06 0.0 4.9995e-06 0.0 5e-06 1.8 5.0195e-06 1.8 5.02e-06 0.0 5.0395e-06 0.0
+ 5.04e-06 1.8 5.0595e-06 1.8 5.06e-06 0.0 5.0795e-06 0.0 5.08e-06 1.8 5.0995e-06 1.8 5.1e-06 0.0 5.12e-06
+ 0.0)
Vb0 b0 0 pwl(0 0.0 2.5595e-06 0.0 2.56e-06 1.8 5.12e-06 1.8)
.ends

.end
